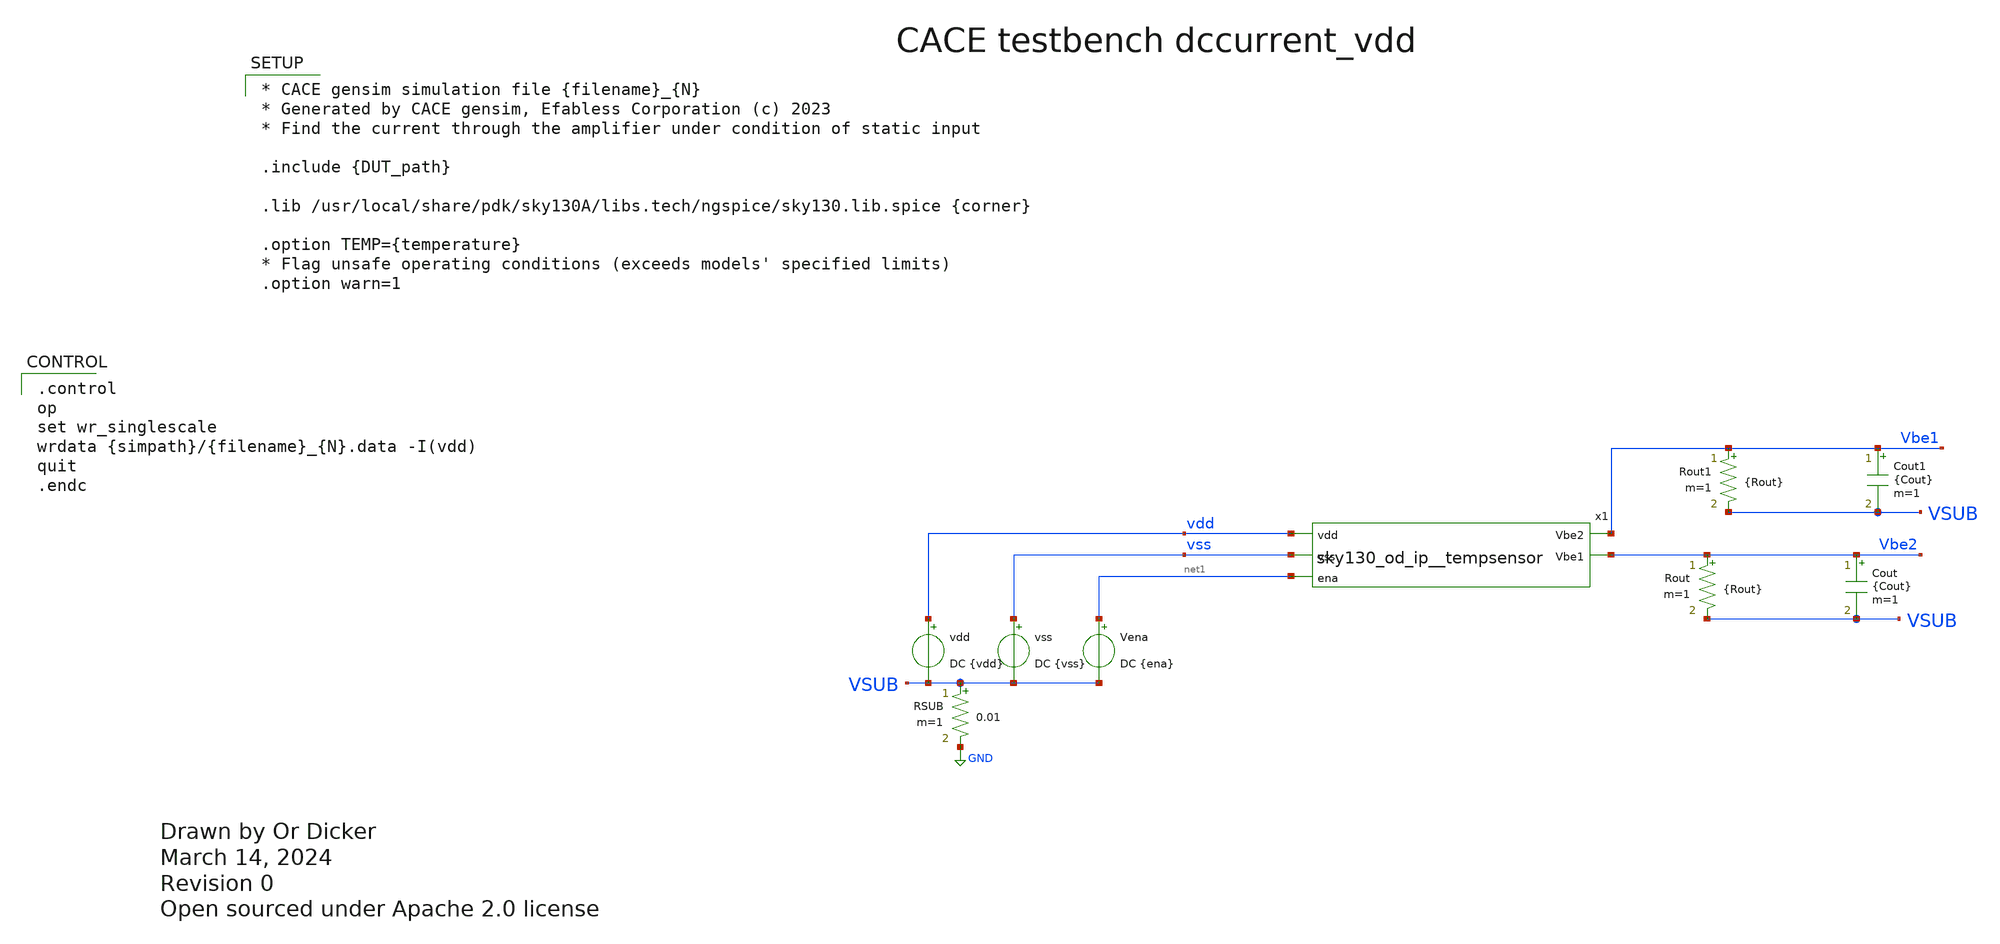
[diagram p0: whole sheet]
** sch_path: cace/dccurrent_vdd.sch
* Open sourced under Apache 2.0 license
**.subckt dccurrent_vdd
vss vss VSUB DC {vss}
Rout Vbe2 VSUB {Rout} m=1
Cout Vbe2 VSUB {Cout} m=1
vdd vdd VSUB DC {vdd}
RSUB VSUB GND 0.01 m=1
x1 vdd vss Vbe1 Vbe2 net1 sky130_od_ip__tempsensor
Rout1 Vbe1 VSUB {Rout} m=1
Cout1 Vbe1 VSUB {Cout} m=1
Vena net1 VSUB DC {ena}
**** begin user architecture code

.control
op
set wr_singlescale
wrdata {simpath}/{filename}_{N}.data -I(vdd)
quit
.endc



* CACE gensim simulation file {filename}_{N}
* Generated by CACE gensim, Efabless Corporation (c) 2023
* Find the current through the amplifier under condition of static input

.include {DUT_path}

.lib /usr/local/share/pdk/sky130A/libs.tech/ngspice/sky130.lib.spice {corner}

.option TEMP={temperature}
* Flag unsafe operating conditions (exceeds models' specified limits)
.option warn=1


**** end user architecture code
**.ends
.GLOBAL GND
.end
